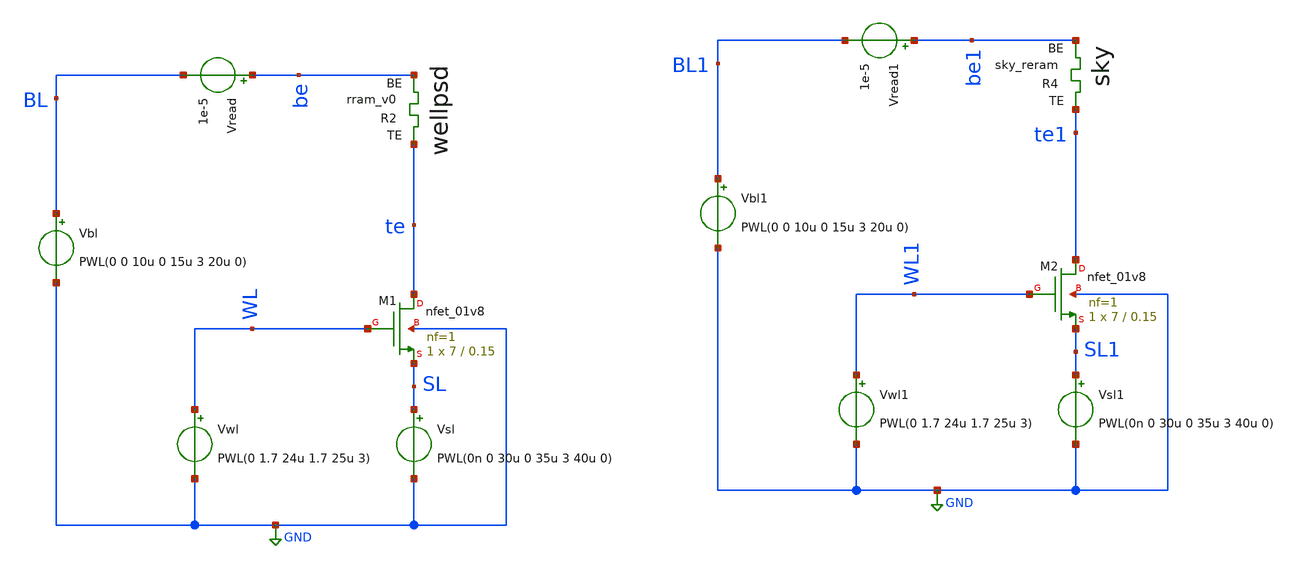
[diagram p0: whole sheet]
** sch_path: Memristor/tb_1T1R_rram_v0.sch
**.subckt tb_1T1R_rram_v0
XM1 te WL SL GND sky130_fd_pr__nfet_01v8 L=0.15 W=7 nf=1 ad='int((nf+1)/2) * W/nf * 0.29' as='int((nf+2)/2) * W/nf * 0.29'
+ pd='2*int((nf+1)/2) * (W/nf + 0.29)' ps='2*int((nf+2)/2) * (W/nf + 0.29)' nrd='0.29 / W' nrs='0.29 / W'
+ sa=0 sb=0 sd=0 mult=1 m=1
Vwl WL GND PWL(0 1.7 24u 1.7 25u 3)
Vbl BL GND PWL(0 0 10u 0 15u 3 20u 0)
Vread be BL 1e-5
Vsl SL GND PWL(0n 0 30u 0 35u 3 40u 0)
XR2 te be rram_v0
XM2 te1 WL1 SL1 GND sky130_fd_pr__nfet_01v8 L=0.15 W=7 nf=1 ad='int((nf+1)/2) * W/nf * 0.29' as='int((nf+2)/2) * W/nf * 0.29'
+ pd='2*int((nf+1)/2) * (W/nf + 0.29)' ps='2*int((nf+2)/2) * (W/nf + 0.29)' nrd='0.29 / W' nrs='0.29 / W'
+ sa=0 sb=0 sd=0 mult=1 m=1
Vwl1 WL1 GND PWL(0 1.7 24u 1.7 25u 3)
Vbl1 BL1 GND PWL(0 0 10u 0 15u 3 20u 0)
Vread1 be1 BL1 1e-5
Vsl1 SL1 GND PWL(0n 0 30u 0 35u 3 40u 0)
XR4 te1 be1 sky_reram
**** begin user architecture code


.options num_threads=8
.control
  save all
  tran 100n 50u uic
  write tb_1T1R_rram_v0.raw
.endc



.lib $::SKYWATER_MODELS/sky130.lib.spice tt

*MADE BY JORGE ALEJANDRO JUAREZ LORA IPN

.subckt rram_v0 TE BE
*N1 TE BE rram_v0_model gap_initial=unif(0.9,0.8)
N1 TE BE rram_v0_model
.ends rram_v0



.subckt sky_reram TE BE
N1 TE BE sky_reram_model Tfilament_0=3.3e-9
.ends sky_reram

.model rram_v0_model rram_v0_va
.model sky_reram_model sky130_fd_pr_reram__reram_cell

.control
pre_osdi /foss/designs/SNN-MWIP/Memristor/rram_v0.osdi
pre_osdi /foss/designs/SNN-MWIP/Memristor/sky.osdi
.endc

**** end user architecture code
**.ends
.GLOBAL GND
.end
